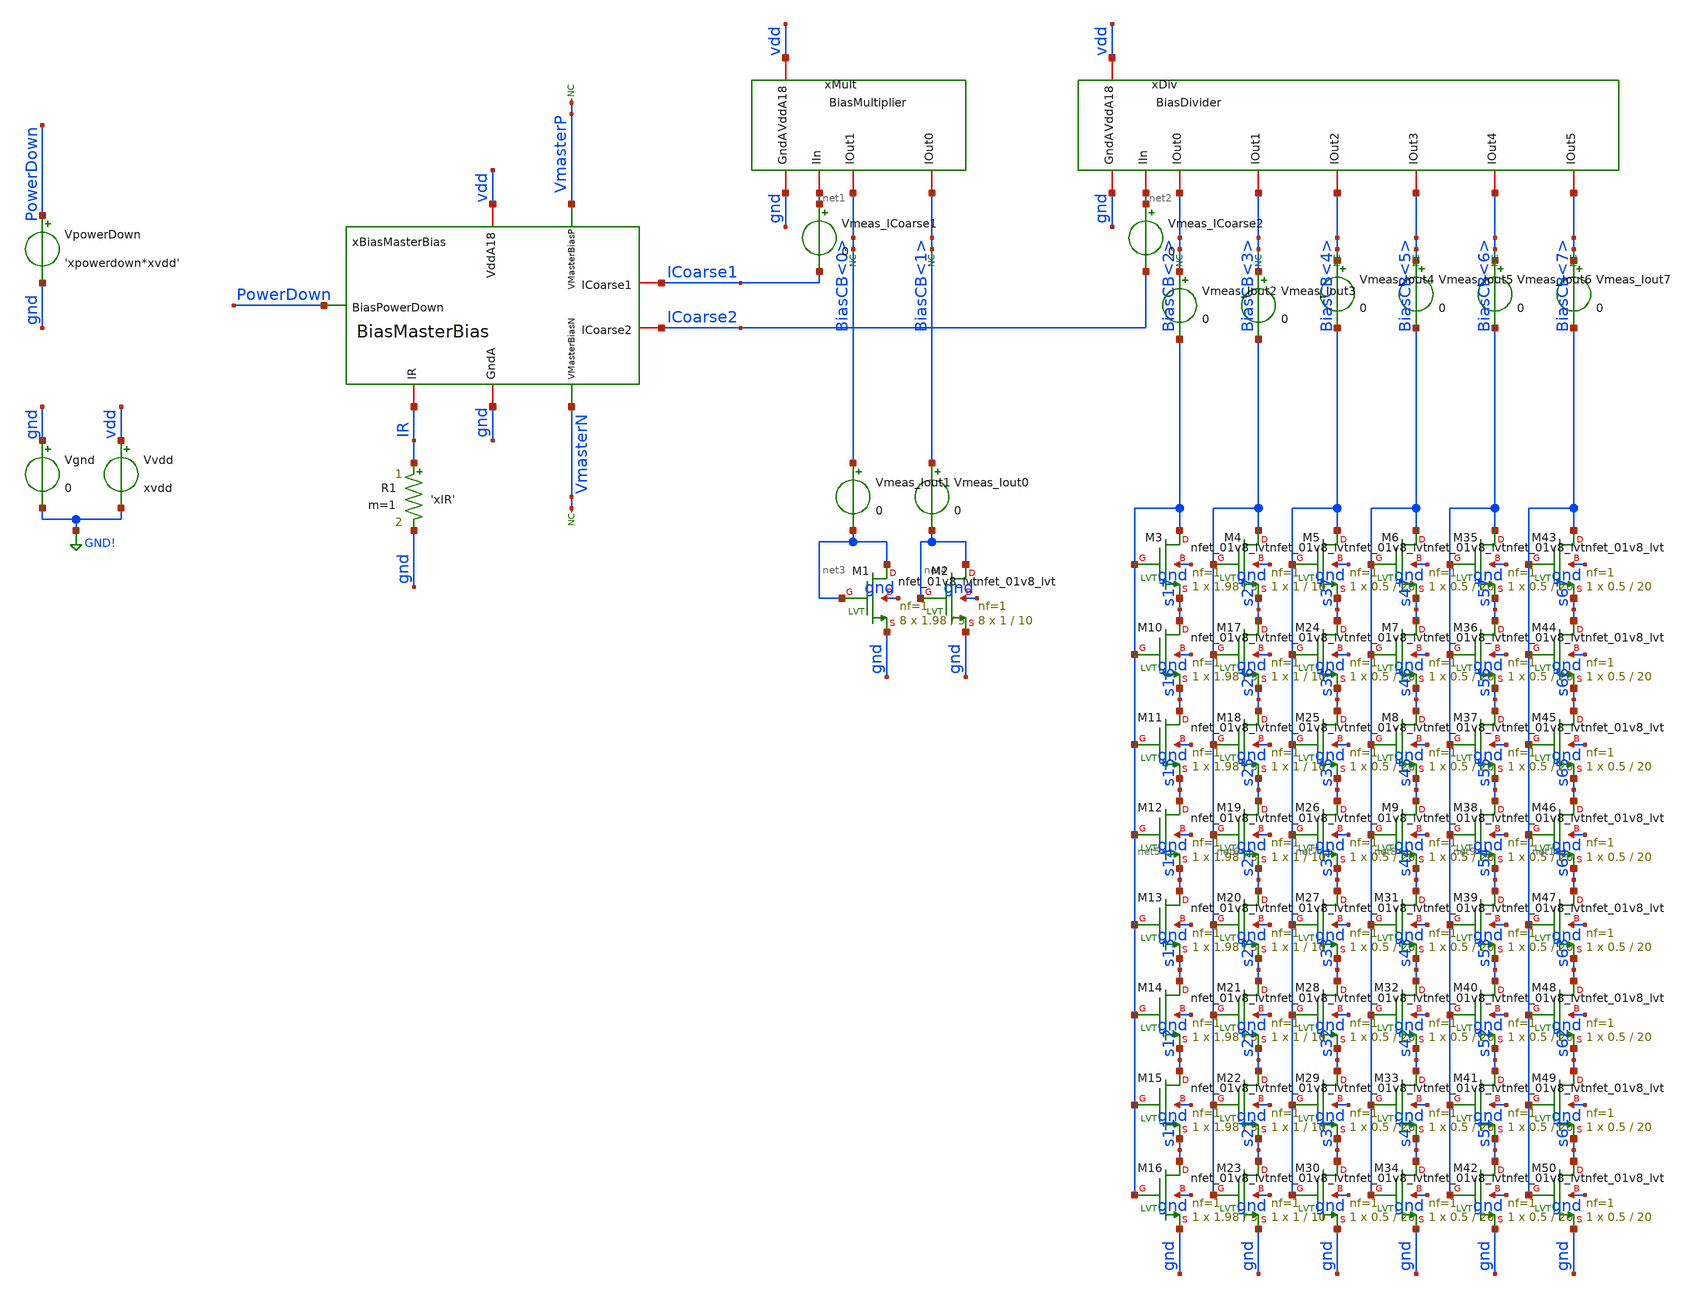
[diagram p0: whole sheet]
** sch_path: analog/xschem/tb_BiasMasterBias.sch
**.subckt tb_BiasMasterBias
Vgnd gnd GND! 0
.save i(vgnd)
Vvdd vdd GND! xvdd
.save i(vvdd)
R1 IR gnd 'xIR' m=1
VpowerDown PowerDown gnd 'xpowerdown*xvdd'
.save i(vpowerdown)
* noconn VmasterN
* noconn VmasterP
* noconn BiasCB<7>
* noconn BiasCB<6>
* noconn BiasCB<5>
* noconn BiasCB<4>
* noconn BiasCB<3>
* noconn BiasCB<2>
* noconn BiasCB<1>
* noconn BiasCB<0>
xBiasMasterBias VmasterP ICoarse2 ICoarse1 VmasterN PowerDown vdd gnd IR BiasMasterBias
xMult gnd vdd net1 BiasCB<0> BiasCB<1> BiasMultiplier
xDiv gnd vdd net2 BiasCB<2> BiasCB<3> BiasCB<4> BiasCB<5> BiasCB<6> BiasCB<7> BiasDivider
Vmeas_ICoarse1 net1 ICoarse1 0
.save i(vmeas_icoarse1)
Vmeas_ICoarse2 net2 ICoarse2 0
.save i(vmeas_icoarse2)
XM1 net3 net3 gnd gnd sky130_fd_pr__nfet_01v8_lvt L=5 W=1.98 nf=1 ad='int((1 + 1)/2) * 1.98 / 1 * 0.29'
+ as='int((1 + 2)/2) * 1.98 / 1 * 0.29' pd='2*int((1 + 1)/2) * (1.98 / 1 + 0.29)' ps='2*int((1 + 2)/2) * (1.98 / 1 + 0.29)'
+ nrd='0.29 / 1.98 ' nrs='0.29 / 1.98 ' sa=0 sb=0 sd=0 mult=8 m=8
XM2 net4 net4 gnd gnd sky130_fd_pr__nfet_01v8_lvt L=10 W=1 nf=1 ad='int((1 + 1)/2) * 1 / 1 * 0.29' as='int((1 + 2)/2) * 1 / 1 * 0.29'
+ pd='2*int((1 + 1)/2) * (1 / 1 + 0.29)' ps='2*int((1 + 2)/2) * (1 / 1 + 0.29)' nrd='0.29 / 1 ' nrs='0.29 / 1 '
+ sa=0 sb=0 sd=0 mult=8 m=8
Vmeas_Iout1 BiasCB<0> net3 0
.save i(vmeas_iout1)
Vmeas_Iout0 BiasCB<1> net4 0
.save i(vmeas_iout0)
Vmeas_Iout2 BiasCB<2> net5 0
.save i(vmeas_iout2)
Vmeas_Iout3 BiasCB<3> net6 0
.save i(vmeas_iout3)
XM3 net5 net5 s17 gnd sky130_fd_pr__nfet_01v8_lvt L=5 W=1.98 nf=1 ad='int((1 + 1)/2) * 1.98 / 1 * 0.29'
+ as='int((1 + 2)/2) * 1.98 / 1 * 0.29' pd='2*int((1 + 1)/2) * (1.98 / 1 + 0.29)' ps='2*int((1 + 2)/2) * (1.98 / 1 + 0.29)'
+ nrd='0.29 / 1.98 ' nrs='0.29 / 1.98 ' sa=0 sb=0 sd=0 mult=1 m=1
XM4 net6 net6 s27 gnd sky130_fd_pr__nfet_01v8_lvt L=10 W=1 nf=1 ad='int((1 + 1)/2) * 1 / 1 * 0.29' as='int((1 + 2)/2) * 1 / 1 * 0.29'
+ pd='2*int((1 + 1)/2) * (1 / 1 + 0.29)' ps='2*int((1 + 2)/2) * (1 / 1 + 0.29)' nrd='0.29 / 1 ' nrs='0.29 / 1 '
+ sa=0 sb=0 sd=0 mult=1 m=1
XM5 net7 net7 s37 gnd sky130_fd_pr__nfet_01v8_lvt L=20 W=0.5 nf=1 ad='int((1 + 1)/2) * 0.5 / 1 * 0.29'
+ as='int((1 + 2)/2) * 0.5 / 1 * 0.29' pd='2*int((1 + 1)/2) * (0.5 / 1 + 0.29)' ps='2*int((1 + 2)/2) * (0.5 / 1 + 0.29)'
+ nrd='0.29 / 0.5 ' nrs='0.29 / 0.5 ' sa=0 sb=0 sd=0 mult=1 m=1
XM10 s17 net5 s16 gnd sky130_fd_pr__nfet_01v8_lvt L=5 W=1.98 nf=1 ad='int((1 + 1)/2) * 1.98 / 1 * 0.29'
+ as='int((1 + 2)/2) * 1.98 / 1 * 0.29' pd='2*int((1 + 1)/2) * (1.98 / 1 + 0.29)' ps='2*int((1 + 2)/2) * (1.98 / 1 + 0.29)'
+ nrd='0.29 / 1.98 ' nrs='0.29 / 1.98 ' sa=0 sb=0 sd=0 mult=1 m=1
XM11 s16 net5 s15 gnd sky130_fd_pr__nfet_01v8_lvt L=5 W=1.98 nf=1 ad='int((1 + 1)/2) * 1.98 / 1 * 0.29'
+ as='int((1 + 2)/2) * 1.98 / 1 * 0.29' pd='2*int((1 + 1)/2) * (1.98 / 1 + 0.29)' ps='2*int((1 + 2)/2) * (1.98 / 1 + 0.29)'
+ nrd='0.29 / 1.98 ' nrs='0.29 / 1.98 ' sa=0 sb=0 sd=0 mult=1 m=1
XM12 s15 net5 s14 gnd sky130_fd_pr__nfet_01v8_lvt L=5 W=1.98 nf=1 ad='int((1 + 1)/2) * 1.98 / 1 * 0.29'
+ as='int((1 + 2)/2) * 1.98 / 1 * 0.29' pd='2*int((1 + 1)/2) * (1.98 / 1 + 0.29)' ps='2*int((1 + 2)/2) * (1.98 / 1 + 0.29)'
+ nrd='0.29 / 1.98 ' nrs='0.29 / 1.98 ' sa=0 sb=0 sd=0 mult=1 m=1
XM13 s14 net5 s13 gnd sky130_fd_pr__nfet_01v8_lvt L=5 W=1.98 nf=1 ad='int((1 + 1)/2) * 1.98 / 1 * 0.29'
+ as='int((1 + 2)/2) * 1.98 / 1 * 0.29' pd='2*int((1 + 1)/2) * (1.98 / 1 + 0.29)' ps='2*int((1 + 2)/2) * (1.98 / 1 + 0.29)'
+ nrd='0.29 / 1.98 ' nrs='0.29 / 1.98 ' sa=0 sb=0 sd=0 mult=1 m=1
XM14 s13 net5 s12 gnd sky130_fd_pr__nfet_01v8_lvt L=5 W=1.98 nf=1 ad='int((1 + 1)/2) * 1.98 / 1 * 0.29'
+ as='int((1 + 2)/2) * 1.98 / 1 * 0.29' pd='2*int((1 + 1)/2) * (1.98 / 1 + 0.29)' ps='2*int((1 + 2)/2) * (1.98 / 1 + 0.29)'
+ nrd='0.29 / 1.98 ' nrs='0.29 / 1.98 ' sa=0 sb=0 sd=0 mult=1 m=1
XM15 s12 net5 s11 gnd sky130_fd_pr__nfet_01v8_lvt L=5 W=1.98 nf=1 ad='int((1 + 1)/2) * 1.98 / 1 * 0.29'
+ as='int((1 + 2)/2) * 1.98 / 1 * 0.29' pd='2*int((1 + 1)/2) * (1.98 / 1 + 0.29)' ps='2*int((1 + 2)/2) * (1.98 / 1 + 0.29)'
+ nrd='0.29 / 1.98 ' nrs='0.29 / 1.98 ' sa=0 sb=0 sd=0 mult=1 m=1
XM16 s11 net5 gnd gnd sky130_fd_pr__nfet_01v8_lvt L=5 W=1.98 nf=1 ad='int((1 + 1)/2) * 1.98 / 1 * 0.29'
+ as='int((1 + 2)/2) * 1.98 / 1 * 0.29' pd='2*int((1 + 1)/2) * (1.98 / 1 + 0.29)' ps='2*int((1 + 2)/2) * (1.98 / 1 + 0.29)'
+ nrd='0.29 / 1.98 ' nrs='0.29 / 1.98 ' sa=0 sb=0 sd=0 mult=1 m=1
XM17 s27 net6 s26 gnd sky130_fd_pr__nfet_01v8_lvt L=10 W=1 nf=1 ad='int((1 + 1)/2) * 1 / 1 * 0.29' as='int((1 + 2)/2) * 1 / 1 * 0.29'
+ pd='2*int((1 + 1)/2) * (1 / 1 + 0.29)' ps='2*int((1 + 2)/2) * (1 / 1 + 0.29)' nrd='0.29 / 1 ' nrs='0.29 / 1 '
+ sa=0 sb=0 sd=0 mult=1 m=1
XM18 s26 net6 s25 gnd sky130_fd_pr__nfet_01v8_lvt L=10 W=1 nf=1 ad='int((1 + 1)/2) * 1 / 1 * 0.29' as='int((1 + 2)/2) * 1 / 1 * 0.29'
+ pd='2*int((1 + 1)/2) * (1 / 1 + 0.29)' ps='2*int((1 + 2)/2) * (1 / 1 + 0.29)' nrd='0.29 / 1 ' nrs='0.29 / 1 '
+ sa=0 sb=0 sd=0 mult=1 m=1
XM19 s25 net6 s24 gnd sky130_fd_pr__nfet_01v8_lvt L=10 W=1 nf=1 ad='int((1 + 1)/2) * 1 / 1 * 0.29' as='int((1 + 2)/2) * 1 / 1 * 0.29'
+ pd='2*int((1 + 1)/2) * (1 / 1 + 0.29)' ps='2*int((1 + 2)/2) * (1 / 1 + 0.29)' nrd='0.29 / 1 ' nrs='0.29 / 1 '
+ sa=0 sb=0 sd=0 mult=1 m=1
XM20 s24 net6 s23 gnd sky130_fd_pr__nfet_01v8_lvt L=10 W=1 nf=1 ad='int((1 + 1)/2) * 1 / 1 * 0.29' as='int((1 + 2)/2) * 1 / 1 * 0.29'
+ pd='2*int((1 + 1)/2) * (1 / 1 + 0.29)' ps='2*int((1 + 2)/2) * (1 / 1 + 0.29)' nrd='0.29 / 1 ' nrs='0.29 / 1 '
+ sa=0 sb=0 sd=0 mult=1 m=1
XM21 s23 net6 s22 gnd sky130_fd_pr__nfet_01v8_lvt L=10 W=1 nf=1 ad='int((1 + 1)/2) * 1 / 1 * 0.29' as='int((1 + 2)/2) * 1 / 1 * 0.29'
+ pd='2*int((1 + 1)/2) * (1 / 1 + 0.29)' ps='2*int((1 + 2)/2) * (1 / 1 + 0.29)' nrd='0.29 / 1 ' nrs='0.29 / 1 '
+ sa=0 sb=0 sd=0 mult=1 m=1
XM22 s22 net6 s21 gnd sky130_fd_pr__nfet_01v8_lvt L=10 W=1 nf=1 ad='int((1 + 1)/2) * 1 / 1 * 0.29' as='int((1 + 2)/2) * 1 / 1 * 0.29'
+ pd='2*int((1 + 1)/2) * (1 / 1 + 0.29)' ps='2*int((1 + 2)/2) * (1 / 1 + 0.29)' nrd='0.29 / 1 ' nrs='0.29 / 1 '
+ sa=0 sb=0 sd=0 mult=1 m=1
XM23 s21 net6 gnd gnd sky130_fd_pr__nfet_01v8_lvt L=10 W=1 nf=1 ad='int((1 + 1)/2) * 1 / 1 * 0.29' as='int((1 + 2)/2) * 1 / 1 * 0.29'
+ pd='2*int((1 + 1)/2) * (1 / 1 + 0.29)' ps='2*int((1 + 2)/2) * (1 / 1 + 0.29)' nrd='0.29 / 1 ' nrs='0.29 / 1 '
+ sa=0 sb=0 sd=0 mult=1 m=1
XM24 s37 net7 s36 gnd sky130_fd_pr__nfet_01v8_lvt L=20 W=0.5 nf=1 ad='int((1 + 1)/2) * 0.5 / 1 * 0.29'
+ as='int((1 + 2)/2) * 0.5 / 1 * 0.29' pd='2*int((1 + 1)/2) * (0.5 / 1 + 0.29)' ps='2*int((1 + 2)/2) * (0.5 / 1 + 0.29)'
+ nrd='0.29 / 0.5 ' nrs='0.29 / 0.5 ' sa=0 sb=0 sd=0 mult=1 m=1
XM25 s36 net7 s35 gnd sky130_fd_pr__nfet_01v8_lvt L=20 W=0.5 nf=1 ad='int((1 + 1)/2) * 0.5 / 1 * 0.29'
+ as='int((1 + 2)/2) * 0.5 / 1 * 0.29' pd='2*int((1 + 1)/2) * (0.5 / 1 + 0.29)' ps='2*int((1 + 2)/2) * (0.5 / 1 + 0.29)'
+ nrd='0.29 / 0.5 ' nrs='0.29 / 0.5 ' sa=0 sb=0 sd=0 mult=1 m=1
XM26 s35 net7 s34 gnd sky130_fd_pr__nfet_01v8_lvt L=20 W=0.5 nf=1 ad='int((1 + 1)/2) * 0.5 / 1 * 0.29'
+ as='int((1 + 2)/2) * 0.5 / 1 * 0.29' pd='2*int((1 + 1)/2) * (0.5 / 1 + 0.29)' ps='2*int((1 + 2)/2) * (0.5 / 1 + 0.29)'
+ nrd='0.29 / 0.5 ' nrs='0.29 / 0.5 ' sa=0 sb=0 sd=0 mult=1 m=1
XM27 s34 net7 s33 gnd sky130_fd_pr__nfet_01v8_lvt L=20 W=0.5 nf=1 ad='int((1 + 1)/2) * 0.5 / 1 * 0.29'
+ as='int((1 + 2)/2) * 0.5 / 1 * 0.29' pd='2*int((1 + 1)/2) * (0.5 / 1 + 0.29)' ps='2*int((1 + 2)/2) * (0.5 / 1 + 0.29)'
+ nrd='0.29 / 0.5 ' nrs='0.29 / 0.5 ' sa=0 sb=0 sd=0 mult=1 m=1
XM28 s33 net7 s32 gnd sky130_fd_pr__nfet_01v8_lvt L=20 W=0.5 nf=1 ad='int((1 + 1)/2) * 0.5 / 1 * 0.29'
+ as='int((1 + 2)/2) * 0.5 / 1 * 0.29' pd='2*int((1 + 1)/2) * (0.5 / 1 + 0.29)' ps='2*int((1 + 2)/2) * (0.5 / 1 + 0.29)'
+ nrd='0.29 / 0.5 ' nrs='0.29 / 0.5 ' sa=0 sb=0 sd=0 mult=1 m=1
XM29 s32 net7 s31 gnd sky130_fd_pr__nfet_01v8_lvt L=20 W=0.5 nf=1 ad='int((1 + 1)/2) * 0.5 / 1 * 0.29'
+ as='int((1 + 2)/2) * 0.5 / 1 * 0.29' pd='2*int((1 + 1)/2) * (0.5 / 1 + 0.29)' ps='2*int((1 + 2)/2) * (0.5 / 1 + 0.29)'
+ nrd='0.29 / 0.5 ' nrs='0.29 / 0.5 ' sa=0 sb=0 sd=0 mult=1 m=1
XM30 s31 net7 gnd gnd sky130_fd_pr__nfet_01v8_lvt L=20 W=0.5 nf=1 ad='int((1 + 1)/2) * 0.5 / 1 * 0.29'
+ as='int((1 + 2)/2) * 0.5 / 1 * 0.29' pd='2*int((1 + 1)/2) * (0.5 / 1 + 0.29)' ps='2*int((1 + 2)/2) * (0.5 / 1 + 0.29)'
+ nrd='0.29 / 0.5 ' nrs='0.29 / 0.5 ' sa=0 sb=0 sd=0 mult=1 m=1
XM6 net8 net8 s47 gnd sky130_fd_pr__nfet_01v8_lvt L=20 W=0.5 nf=1 ad='int((1 + 1)/2) * 0.5 / 1 * 0.29'
+ as='int((1 + 2)/2) * 0.5 / 1 * 0.29' pd='2*int((1 + 1)/2) * (0.5 / 1 + 0.29)' ps='2*int((1 + 2)/2) * (0.5 / 1 + 0.29)'
+ nrd='0.29 / 0.5 ' nrs='0.29 / 0.5 ' sa=0 sb=0 sd=0 mult=1 m=1
XM7 s47 net8 s46 gnd sky130_fd_pr__nfet_01v8_lvt L=20 W=0.5 nf=1 ad='int((1 + 1)/2) * 0.5 / 1 * 0.29'
+ as='int((1 + 2)/2) * 0.5 / 1 * 0.29' pd='2*int((1 + 1)/2) * (0.5 / 1 + 0.29)' ps='2*int((1 + 2)/2) * (0.5 / 1 + 0.29)'
+ nrd='0.29 / 0.5 ' nrs='0.29 / 0.5 ' sa=0 sb=0 sd=0 mult=1 m=1
XM8 s46 net8 s45 gnd sky130_fd_pr__nfet_01v8_lvt L=20 W=0.5 nf=1 ad='int((1 + 1)/2) * 0.5 / 1 * 0.29'
+ as='int((1 + 2)/2) * 0.5 / 1 * 0.29' pd='2*int((1 + 1)/2) * (0.5 / 1 + 0.29)' ps='2*int((1 + 2)/2) * (0.5 / 1 + 0.29)'
+ nrd='0.29 / 0.5 ' nrs='0.29 / 0.5 ' sa=0 sb=0 sd=0 mult=1 m=1
XM9 s45 net8 s44 gnd sky130_fd_pr__nfet_01v8_lvt L=20 W=0.5 nf=1 ad='int((1 + 1)/2) * 0.5 / 1 * 0.29'
+ as='int((1 + 2)/2) * 0.5 / 1 * 0.29' pd='2*int((1 + 1)/2) * (0.5 / 1 + 0.29)' ps='2*int((1 + 2)/2) * (0.5 / 1 + 0.29)'
+ nrd='0.29 / 0.5 ' nrs='0.29 / 0.5 ' sa=0 sb=0 sd=0 mult=1 m=1
XM31 s44 net8 s43 gnd sky130_fd_pr__nfet_01v8_lvt L=20 W=0.5 nf=1 ad='int((1 + 1)/2) * 0.5 / 1 * 0.29'
+ as='int((1 + 2)/2) * 0.5 / 1 * 0.29' pd='2*int((1 + 1)/2) * (0.5 / 1 + 0.29)' ps='2*int((1 + 2)/2) * (0.5 / 1 + 0.29)'
+ nrd='0.29 / 0.5 ' nrs='0.29 / 0.5 ' sa=0 sb=0 sd=0 mult=1 m=1
XM32 s43 net8 s42 gnd sky130_fd_pr__nfet_01v8_lvt L=20 W=0.5 nf=1 ad='int((1 + 1)/2) * 0.5 / 1 * 0.29'
+ as='int((1 + 2)/2) * 0.5 / 1 * 0.29' pd='2*int((1 + 1)/2) * (0.5 / 1 + 0.29)' ps='2*int((1 + 2)/2) * (0.5 / 1 + 0.29)'
+ nrd='0.29 / 0.5 ' nrs='0.29 / 0.5 ' sa=0 sb=0 sd=0 mult=1 m=1
XM33 s42 net8 s41 gnd sky130_fd_pr__nfet_01v8_lvt L=20 W=0.5 nf=1 ad='int((1 + 1)/2) * 0.5 / 1 * 0.29'
+ as='int((1 + 2)/2) * 0.5 / 1 * 0.29' pd='2*int((1 + 1)/2) * (0.5 / 1 + 0.29)' ps='2*int((1 + 2)/2) * (0.5 / 1 + 0.29)'
+ nrd='0.29 / 0.5 ' nrs='0.29 / 0.5 ' sa=0 sb=0 sd=0 mult=1 m=1
XM34 s41 net8 gnd gnd sky130_fd_pr__nfet_01v8_lvt L=20 W=0.5 nf=1 ad='int((1 + 1)/2) * 0.5 / 1 * 0.29'
+ as='int((1 + 2)/2) * 0.5 / 1 * 0.29' pd='2*int((1 + 1)/2) * (0.5 / 1 + 0.29)' ps='2*int((1 + 2)/2) * (0.5 / 1 + 0.29)'
+ nrd='0.29 / 0.5 ' nrs='0.29 / 0.5 ' sa=0 sb=0 sd=0 mult=1 m=1
XM35 net9 net9 s57 gnd sky130_fd_pr__nfet_01v8_lvt L=20 W=0.5 nf=1 ad='int((1 + 1)/2) * 0.5 / 1 * 0.29'
+ as='int((1 + 2)/2) * 0.5 / 1 * 0.29' pd='2*int((1 + 1)/2) * (0.5 / 1 + 0.29)' ps='2*int((1 + 2)/2) * (0.5 / 1 + 0.29)'
+ nrd='0.29 / 0.5 ' nrs='0.29 / 0.5 ' sa=0 sb=0 sd=0 mult=1 m=1
XM36 s57 net9 s56 gnd sky130_fd_pr__nfet_01v8_lvt L=20 W=0.5 nf=1 ad='int((1 + 1)/2) * 0.5 / 1 * 0.29'
+ as='int((1 + 2)/2) * 0.5 / 1 * 0.29' pd='2*int((1 + 1)/2) * (0.5 / 1 + 0.29)' ps='2*int((1 + 2)/2) * (0.5 / 1 + 0.29)'
+ nrd='0.29 / 0.5 ' nrs='0.29 / 0.5 ' sa=0 sb=0 sd=0 mult=1 m=1
XM37 s56 net9 s55 gnd sky130_fd_pr__nfet_01v8_lvt L=20 W=0.5 nf=1 ad='int((1 + 1)/2) * 0.5 / 1 * 0.29'
+ as='int((1 + 2)/2) * 0.5 / 1 * 0.29' pd='2*int((1 + 1)/2) * (0.5 / 1 + 0.29)' ps='2*int((1 + 2)/2) * (0.5 / 1 + 0.29)'
+ nrd='0.29 / 0.5 ' nrs='0.29 / 0.5 ' sa=0 sb=0 sd=0 mult=1 m=1
XM38 s55 net9 s54 gnd sky130_fd_pr__nfet_01v8_lvt L=20 W=0.5 nf=1 ad='int((1 + 1)/2) * 0.5 / 1 * 0.29'
+ as='int((1 + 2)/2) * 0.5 / 1 * 0.29' pd='2*int((1 + 1)/2) * (0.5 / 1 + 0.29)' ps='2*int((1 + 2)/2) * (0.5 / 1 + 0.29)'
+ nrd='0.29 / 0.5 ' nrs='0.29 / 0.5 ' sa=0 sb=0 sd=0 mult=1 m=1
XM39 s54 net9 s53 gnd sky130_fd_pr__nfet_01v8_lvt L=20 W=0.5 nf=1 ad='int((1 + 1)/2) * 0.5 / 1 * 0.29'
+ as='int((1 + 2)/2) * 0.5 / 1 * 0.29' pd='2*int((1 + 1)/2) * (0.5 / 1 + 0.29)' ps='2*int((1 + 2)/2) * (0.5 / 1 + 0.29)'
+ nrd='0.29 / 0.5 ' nrs='0.29 / 0.5 ' sa=0 sb=0 sd=0 mult=1 m=1
XM40 s53 net9 s52 gnd sky130_fd_pr__nfet_01v8_lvt L=20 W=0.5 nf=1 ad='int((1 + 1)/2) * 0.5 / 1 * 0.29'
+ as='int((1 + 2)/2) * 0.5 / 1 * 0.29' pd='2*int((1 + 1)/2) * (0.5 / 1 + 0.29)' ps='2*int((1 + 2)/2) * (0.5 / 1 + 0.29)'
+ nrd='0.29 / 0.5 ' nrs='0.29 / 0.5 ' sa=0 sb=0 sd=0 mult=1 m=1
XM41 s52 net9 s51 gnd sky130_fd_pr__nfet_01v8_lvt L=20 W=0.5 nf=1 ad='int((1 + 1)/2) * 0.5 / 1 * 0.29'
+ as='int((1 + 2)/2) * 0.5 / 1 * 0.29' pd='2*int((1 + 1)/2) * (0.5 / 1 + 0.29)' ps='2*int((1 + 2)/2) * (0.5 / 1 + 0.29)'
+ nrd='0.29 / 0.5 ' nrs='0.29 / 0.5 ' sa=0 sb=0 sd=0 mult=1 m=1
XM42 s51 net9 gnd gnd sky130_fd_pr__nfet_01v8_lvt L=20 W=0.5 nf=1 ad='int((1 + 1)/2) * 0.5 / 1 * 0.29'
+ as='int((1 + 2)/2) * 0.5 / 1 * 0.29' pd='2*int((1 + 1)/2) * (0.5 / 1 + 0.29)' ps='2*int((1 + 2)/2) * (0.5 / 1 + 0.29)'
+ nrd='0.29 / 0.5 ' nrs='0.29 / 0.5 ' sa=0 sb=0 sd=0 mult=1 m=1
XM43 net10 net10 s67 gnd sky130_fd_pr__nfet_01v8_lvt L=20 W=0.5 nf=1 ad='int((1 + 1)/2) * 0.5 / 1 * 0.29'
+ as='int((1 + 2)/2) * 0.5 / 1 * 0.29' pd='2*int((1 + 1)/2) * (0.5 / 1 + 0.29)' ps='2*int((1 + 2)/2) * (0.5 / 1 + 0.29)'
+ nrd='0.29 / 0.5 ' nrs='0.29 / 0.5 ' sa=0 sb=0 sd=0 mult=1 m=1
XM44 s67 net10 s66 gnd sky130_fd_pr__nfet_01v8_lvt L=20 W=0.5 nf=1 ad='int((1 + 1)/2) * 0.5 / 1 * 0.29'
+ as='int((1 + 2)/2) * 0.5 / 1 * 0.29' pd='2*int((1 + 1)/2) * (0.5 / 1 + 0.29)' ps='2*int((1 + 2)/2) * (0.5 / 1 + 0.29)'
+ nrd='0.29 / 0.5 ' nrs='0.29 / 0.5 ' sa=0 sb=0 sd=0 mult=1 m=1
XM45 s66 net10 s65 gnd sky130_fd_pr__nfet_01v8_lvt L=20 W=0.5 nf=1 ad='int((1 + 1)/2) * 0.5 / 1 * 0.29'
+ as='int((1 + 2)/2) * 0.5 / 1 * 0.29' pd='2*int((1 + 1)/2) * (0.5 / 1 + 0.29)' ps='2*int((1 + 2)/2) * (0.5 / 1 + 0.29)'
+ nrd='0.29 / 0.5 ' nrs='0.29 / 0.5 ' sa=0 sb=0 sd=0 mult=1 m=1
XM46 s65 net10 s64 gnd sky130_fd_pr__nfet_01v8_lvt L=20 W=0.5 nf=1 ad='int((1 + 1)/2) * 0.5 / 1 * 0.29'
+ as='int((1 + 2)/2) * 0.5 / 1 * 0.29' pd='2*int((1 + 1)/2) * (0.5 / 1 + 0.29)' ps='2*int((1 + 2)/2) * (0.5 / 1 + 0.29)'
+ nrd='0.29 / 0.5 ' nrs='0.29 / 0.5 ' sa=0 sb=0 sd=0 mult=1 m=1
XM47 s64 net10 s63 gnd sky130_fd_pr__nfet_01v8_lvt L=20 W=0.5 nf=1 ad='int((1 + 1)/2) * 0.5 / 1 * 0.29'
+ as='int((1 + 2)/2) * 0.5 / 1 * 0.29' pd='2*int((1 + 1)/2) * (0.5 / 1 + 0.29)' ps='2*int((1 + 2)/2) * (0.5 / 1 + 0.29)'
+ nrd='0.29 / 0.5 ' nrs='0.29 / 0.5 ' sa=0 sb=0 sd=0 mult=1 m=1
XM48 s63 net10 s62 gnd sky130_fd_pr__nfet_01v8_lvt L=20 W=0.5 nf=1 ad='int((1 + 1)/2) * 0.5 / 1 * 0.29'
+ as='int((1 + 2)/2) * 0.5 / 1 * 0.29' pd='2*int((1 + 1)/2) * (0.5 / 1 + 0.29)' ps='2*int((1 + 2)/2) * (0.5 / 1 + 0.29)'
+ nrd='0.29 / 0.5 ' nrs='0.29 / 0.5 ' sa=0 sb=0 sd=0 mult=1 m=1
XM49 s62 net10 s61 gnd sky130_fd_pr__nfet_01v8_lvt L=20 W=0.5 nf=1 ad='int((1 + 1)/2) * 0.5 / 1 * 0.29'
+ as='int((1 + 2)/2) * 0.5 / 1 * 0.29' pd='2*int((1 + 1)/2) * (0.5 / 1 + 0.29)' ps='2*int((1 + 2)/2) * (0.5 / 1 + 0.29)'
+ nrd='0.29 / 0.5 ' nrs='0.29 / 0.5 ' sa=0 sb=0 sd=0 mult=1 m=1
XM50 s61 net10 gnd gnd sky130_fd_pr__nfet_01v8_lvt L=20 W=0.5 nf=1 ad='int((1 + 1)/2) * 0.5 / 1 * 0.29'
+ as='int((1 + 2)/2) * 0.5 / 1 * 0.29' pd='2*int((1 + 1)/2) * (0.5 / 1 + 0.29)' ps='2*int((1 + 2)/2) * (0.5 / 1 + 0.29)'
+ nrd='0.29 / 0.5 ' nrs='0.29 / 0.5 ' sa=0 sb=0 sd=0 mult=1 m=1
Vmeas_Iout4 BiasCB<4> net7 0
.save i(vmeas_iout4)
Vmeas_Iout5 BiasCB<5> net8 0
.save i(vmeas_iout5)
Vmeas_Iout6 BiasCB<6> net9 0
.save i(vmeas_iout6)
Vmeas_Iout7 BiasCB<7> net10 0
.save i(vmeas_iout7)
**** begin user architecture code

** opencircuitdesign pdks install
.lib $::SKYWATER_MODELS/sky130.lib.spice tt



.param xvdd = 1.8
.param xpowerdown = 0
.param xIR = 100k
.save all
.probe alli
.probe i(xMasterBias.xmnbias:d)
.save i(xMasterBias.xmnbias:d)
.save i(xMasterBias.xmnbias,d)
.op



**** end user architecture code
**.ends
.GLOBAL GND!
.end
